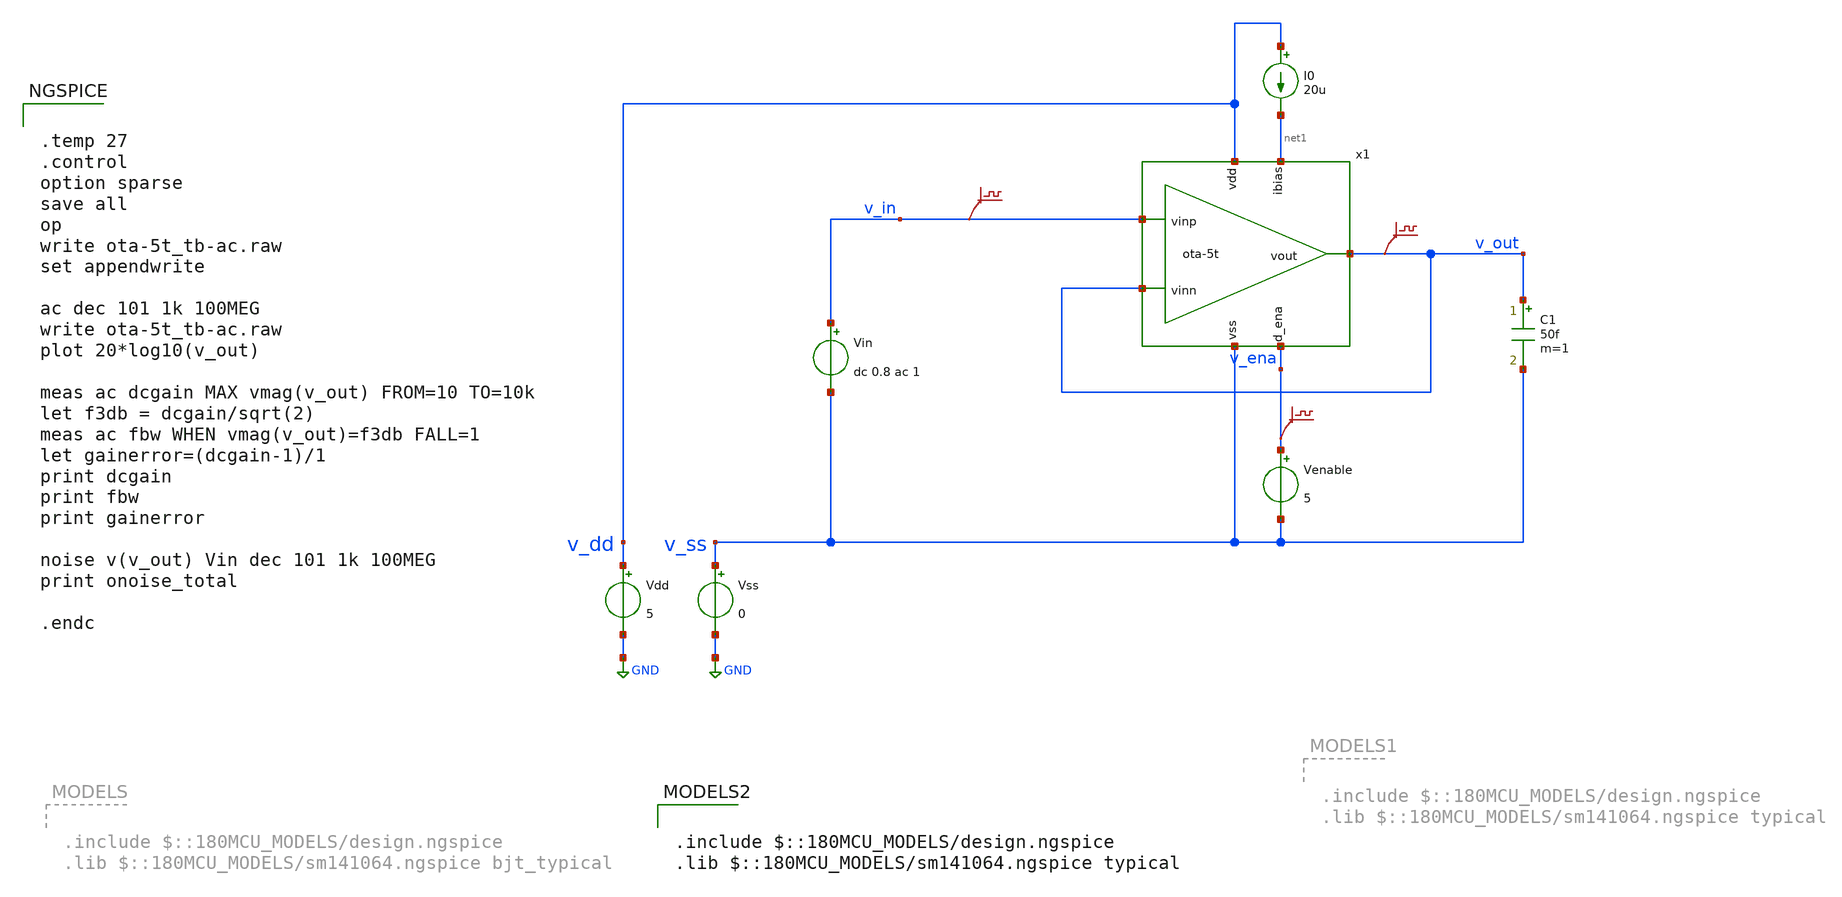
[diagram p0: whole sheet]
** sch_path: xschem/ota-5t_tb-ac.sch
**.subckt ota-5t_tb-ac
Vdd v_dd GND 5
Vss v_ss GND 0
C1 v_out v_ss 50f m=1
Vin v_in v_ss dc 0.8 ac 1
I0 v_dd net1 20u
Venable v_ena v_ss 5
.save v(v_in)
.save v(v_out)
.save v(v_ena)
x1 v_dd v_out v_in v_out net1 v_ena v_ss ota-5t
**** begin user architecture code


.temp 27
.control
option sparse
save all
op
write ota-5t_tb-ac.raw
set appendwrite

ac dec 101 1k 100MEG
write ota-5t_tb-ac.raw
plot 20*log10(v_out)

meas ac dcgain MAX vmag(v_out) FROM=10 TO=10k
let f3db = dcgain/sqrt(2)
meas ac fbw WHEN vmag(v_out)=f3db FALL=1
let gainerror=(dcgain-1)/1
print dcgain
print fbw
print gainerror

noise v(v_out) Vin dec 101 1k 100MEG
print onoise_total

.endc



.include $::180MCU_MODELS/design.ngspice
.lib $::180MCU_MODELS/sm141064.ngspice typical

**** end user architecture code
**.ends
.GLOBAL GND
.end
